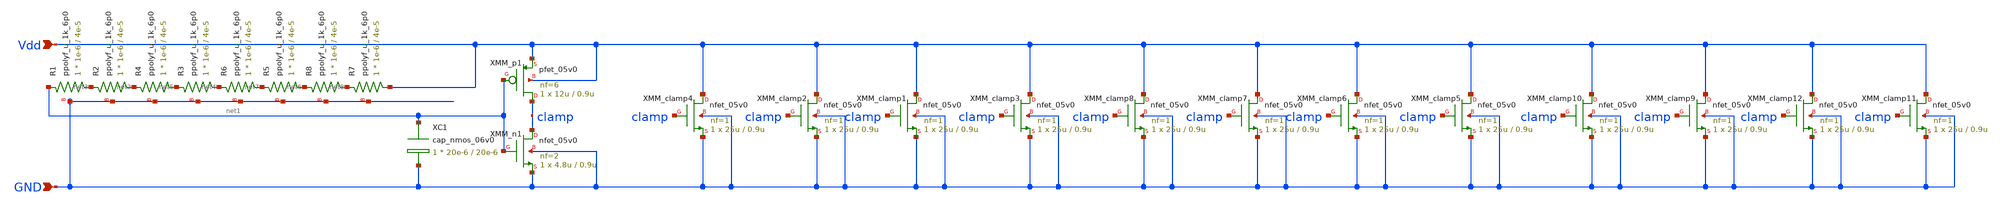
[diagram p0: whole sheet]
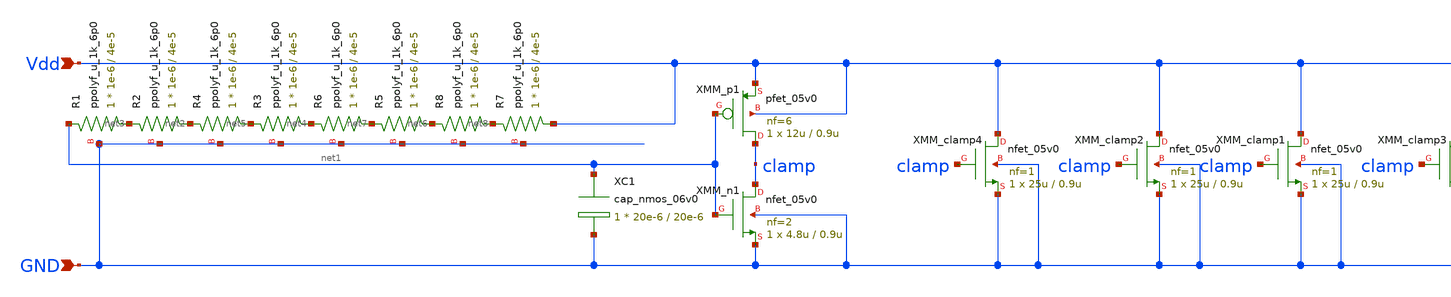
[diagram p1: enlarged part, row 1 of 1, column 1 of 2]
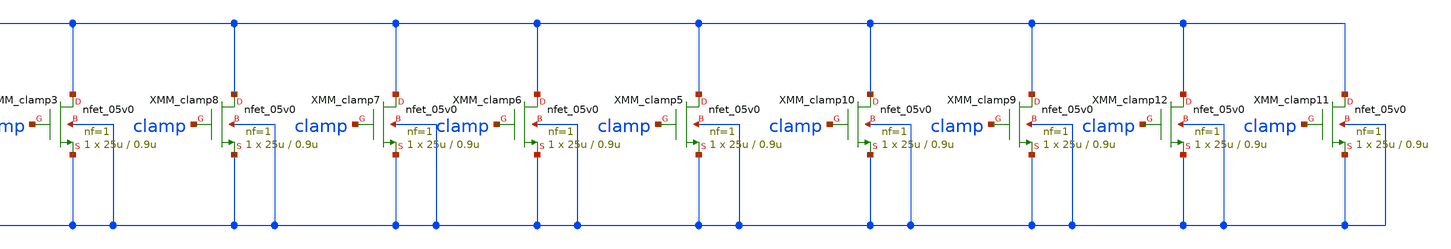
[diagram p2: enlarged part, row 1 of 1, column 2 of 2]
** sch_path: MG_ESD_protection/MG_power_clamp_ESD.sch
**.subckt MG_power_clamp_ESD Vdd GND
*.ipin Vdd
*.ipin GND
XMM_p1 clamp net1 Vdd Vdd pfet_05v0 L=0.9u W=12u nf=6 ad='int((nf+1)/2) * W/nf * 0.18u' as='int((nf+2)/2) * W/nf * 0.18u'
+ pd='2*int((nf+1)/2) * (W/nf + 0.18u)' ps='2*int((nf+2)/2) * (W/nf + 0.18u)' nrd='0.18u / W' nrs='0.18u / W'
+ sa=0 sb=0 sd=0 m=1
XMM_n1 clamp net1 GND GND nfet_05v0 L=0.9u W=4.8u nf=2 ad='int((nf+1)/2) * W/nf * 0.18u' as='int((nf+2)/2) * W/nf * 0.18u'
+ pd='2*int((nf+1)/2) * (W/nf + 0.18u)' ps='2*int((nf+2)/2) * (W/nf + 0.18u)' nrd='0.18u / W' nrs='0.18u / W'
+ sa=0 sb=0 sd=0 m=1
XC1 net1 GND cap_nmos_06v0 c_width=20e-6 c_length=20e-6 m=1
XMM_clamp3 Vdd clamp GND GND nfet_05v0 L=0.9u W=25u nf=1 ad='int((nf+1)/2) * W/nf * 0.18u' as='int((nf+2)/2) * W/nf * 0.18u'
+ pd='2*int((nf+1)/2) * (W/nf + 0.18u)' ps='2*int((nf+2)/2) * (W/nf + 0.18u)' nrd='0.18u / W' nrs='0.18u / W'
+ sa=0 sb=0 sd=0 m=1
XR2 net2 net3 GND ppolyf_u_1k_6p0 r_width=1e-6 r_length=4e-5 m=1
XR1 net3 net1 GND ppolyf_u_1k_6p0 r_width=1e-6 r_length=4e-5 m=1
XR3 net4 net5 GND ppolyf_u_1k_6p0 r_width=1e-6 r_length=4e-5 m=1
XR4 net5 net2 GND ppolyf_u_1k_6p0 r_width=1e-6 r_length=4e-5 m=1
XR5 net6 net7 GND ppolyf_u_1k_6p0 r_width=1e-6 r_length=4e-5 m=1
XR6 net7 net4 GND ppolyf_u_1k_6p0 r_width=1e-6 r_length=4e-5 m=1
XR7 Vdd net8 GND ppolyf_u_1k_6p0 r_width=1e-6 r_length=4e-5 m=1
XR8 net8 net6 GND ppolyf_u_1k_6p0 r_width=1e-6 r_length=4e-5 m=1
XMM_clamp1 Vdd clamp GND GND nfet_05v0 L=0.9u W=25u nf=1 ad='int((nf+1)/2) * W/nf * 0.18u' as='int((nf+2)/2) * W/nf * 0.18u'
+ pd='2*int((nf+1)/2) * (W/nf + 0.18u)' ps='2*int((nf+2)/2) * (W/nf + 0.18u)' nrd='0.18u / W' nrs='0.18u / W'
+ sa=0 sb=0 sd=0 m=1
XMM_clamp2 Vdd clamp GND GND nfet_05v0 L=0.9u W=25u nf=1 ad='int((nf+1)/2) * W/nf * 0.18u' as='int((nf+2)/2) * W/nf * 0.18u'
+ pd='2*int((nf+1)/2) * (W/nf + 0.18u)' ps='2*int((nf+2)/2) * (W/nf + 0.18u)' nrd='0.18u / W' nrs='0.18u / W'
+ sa=0 sb=0 sd=0 m=1
XMM_clamp4 Vdd clamp GND GND nfet_05v0 L=0.9u W=25u nf=1 ad='int((nf+1)/2) * W/nf * 0.18u' as='int((nf+2)/2) * W/nf * 0.18u'
+ pd='2*int((nf+1)/2) * (W/nf + 0.18u)' ps='2*int((nf+2)/2) * (W/nf + 0.18u)' nrd='0.18u / W' nrs='0.18u / W'
+ sa=0 sb=0 sd=0 m=1
XMM_clamp5 Vdd clamp GND GND nfet_05v0 L=0.9u W=25u nf=1 ad='int((nf+1)/2) * W/nf * 0.18u' as='int((nf+2)/2) * W/nf * 0.18u'
+ pd='2*int((nf+1)/2) * (W/nf + 0.18u)' ps='2*int((nf+2)/2) * (W/nf + 0.18u)' nrd='0.18u / W' nrs='0.18u / W'
+ sa=0 sb=0 sd=0 m=1
XMM_clamp6 Vdd clamp GND GND nfet_05v0 L=0.9u W=25u nf=1 ad='int((nf+1)/2) * W/nf * 0.18u' as='int((nf+2)/2) * W/nf * 0.18u'
+ pd='2*int((nf+1)/2) * (W/nf + 0.18u)' ps='2*int((nf+2)/2) * (W/nf + 0.18u)' nrd='0.18u / W' nrs='0.18u / W'
+ sa=0 sb=0 sd=0 m=1
XMM_clamp7 Vdd clamp GND GND nfet_05v0 L=0.9u W=25u nf=1 ad='int((nf+1)/2) * W/nf * 0.18u' as='int((nf+2)/2) * W/nf * 0.18u'
+ pd='2*int((nf+1)/2) * (W/nf + 0.18u)' ps='2*int((nf+2)/2) * (W/nf + 0.18u)' nrd='0.18u / W' nrs='0.18u / W'
+ sa=0 sb=0 sd=0 m=1
XMM_clamp8 Vdd clamp GND GND nfet_05v0 L=0.9u W=25u nf=1 ad='int((nf+1)/2) * W/nf * 0.18u' as='int((nf+2)/2) * W/nf * 0.18u'
+ pd='2*int((nf+1)/2) * (W/nf + 0.18u)' ps='2*int((nf+2)/2) * (W/nf + 0.18u)' nrd='0.18u / W' nrs='0.18u / W'
+ sa=0 sb=0 sd=0 m=1
XMM_clamp9 Vdd clamp GND GND nfet_05v0 L=0.9u W=25u nf=1 ad='int((nf+1)/2) * W/nf * 0.18u' as='int((nf+2)/2) * W/nf * 0.18u'
+ pd='2*int((nf+1)/2) * (W/nf + 0.18u)' ps='2*int((nf+2)/2) * (W/nf + 0.18u)' nrd='0.18u / W' nrs='0.18u / W'
+ sa=0 sb=0 sd=0 m=1
XMM_clamp10 Vdd clamp GND GND nfet_05v0 L=0.9u W=25u nf=1 ad='int((nf+1)/2) * W/nf * 0.18u' as='int((nf+2)/2) * W/nf * 0.18u'
+ pd='2*int((nf+1)/2) * (W/nf + 0.18u)' ps='2*int((nf+2)/2) * (W/nf + 0.18u)' nrd='0.18u / W' nrs='0.18u / W'
+ sa=0 sb=0 sd=0 m=1
XMM_clamp11 Vdd clamp GND GND nfet_05v0 L=0.9u W=25u nf=1 ad='int((nf+1)/2) * W/nf * 0.18u' as='int((nf+2)/2) * W/nf * 0.18u'
+ pd='2*int((nf+1)/2) * (W/nf + 0.18u)' ps='2*int((nf+2)/2) * (W/nf + 0.18u)' nrd='0.18u / W' nrs='0.18u / W'
+ sa=0 sb=0 sd=0 m=1
XMM_clamp12 Vdd clamp GND GND nfet_05v0 L=0.9u W=25u nf=1 ad='int((nf+1)/2) * W/nf * 0.18u' as='int((nf+2)/2) * W/nf * 0.18u'
+ pd='2*int((nf+1)/2) * (W/nf + 0.18u)' ps='2*int((nf+2)/2) * (W/nf + 0.18u)' nrd='0.18u / W' nrs='0.18u / W'
+ sa=0 sb=0 sd=0 m=1
**.ends
.end
